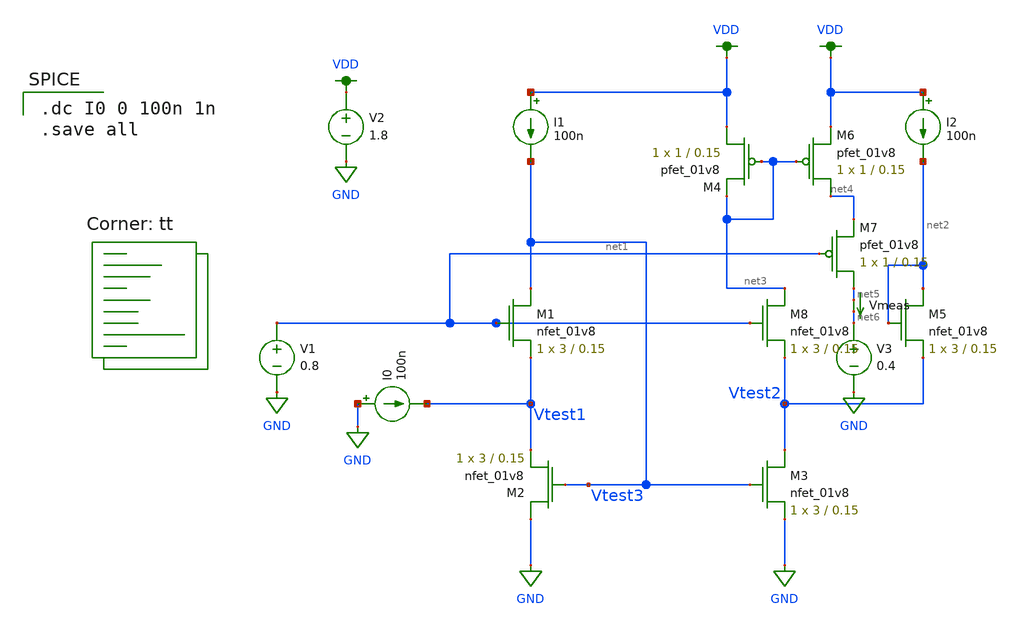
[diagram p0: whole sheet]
** sch_path: test_fvfccm.sch
**.subckt test_fvfccm
XM1 Vtest3 net1 Vtest1 GND sky130_fd_pr__nfet_01v8 L=0.15 W=3 nf=1 ad='int((nf+1)/2) * W/nf * 0.29' as='int((nf+2)/2) * W/nf * 0.29'
+ pd='2*int((nf+1)/2) * (W/nf + 0.29)' ps='2*int((nf+2)/2) * (W/nf + 0.29)' nrd='0.29 / W' nrs='0.29 / W'
+ sa=0 sb=0 sd=0 mult=1 m=1
XM2 GND Vtest3 Vtest1 GND sky130_fd_pr__nfet_01v8 L=0.15 W=3 nf=1 ad='int((nf+1)/2) * W/nf * 0.29' as='int((nf+2)/2) * W/nf * 0.29'
+ pd='2*int((nf+1)/2) * (W/nf + 0.29)' ps='2*int((nf+2)/2) * (W/nf + 0.29)' nrd='0.29 / W' nrs='0.29 / W'
+ sa=0 sb=0 sd=0 mult=1 m=1
I0 GND Vtest1 100n
V1 net1 GND 0.8
I1 VDD Vtest3 100n
V2 VDD GND 1.8
XM3 Vtest2 Vtest3 GND GND sky130_fd_pr__nfet_01v8 L=0.15 W=3 nf=1 ad='int((nf+1)/2) * W/nf * 0.29' as='int((nf+2)/2) * W/nf * 0.29'
+ pd='2*int((nf+1)/2) * (W/nf + 0.29)' ps='2*int((nf+2)/2) * (W/nf + 0.29)' nrd='0.29 / W' nrs='0.29 / W'
+ sa=0 sb=0 sd=0 mult=1 m=1
XM5 net2 net2 Vtest2 GND sky130_fd_pr__nfet_01v8 L=0.15 W=3 nf=1 ad='int((nf+1)/2) * W/nf * 0.29' as='int((nf+2)/2) * W/nf * 0.29'
+ pd='2*int((nf+1)/2) * (W/nf + 0.29)' ps='2*int((nf+2)/2) * (W/nf + 0.29)' nrd='0.29 / W' nrs='0.29 / W'
+ sa=0 sb=0 sd=0 mult=1 m=1
I2 VDD net2 100n
Vmeas net5 net6 0
.save i(vmeas)
XM4 VDD net3 net3 VDD sky130_fd_pr__pfet_01v8 L=0.15 W=1 nf=1 ad='int((nf+1)/2) * W/nf * 0.29' as='int((nf+2)/2) * W/nf * 0.29'
+ pd='2*int((nf+1)/2) * (W/nf + 0.29)' ps='2*int((nf+2)/2) * (W/nf + 0.29)' nrd='0.29 / W' nrs='0.29 / W'
+ sa=0 sb=0 sd=0 mult=1 m=1
XM6 net4 net3 VDD VDD sky130_fd_pr__pfet_01v8 L=0.15 W=1 nf=1 ad='int((nf+1)/2) * W/nf * 0.29' as='int((nf+2)/2) * W/nf * 0.29'
+ pd='2*int((nf+1)/2) * (W/nf + 0.29)' ps='2*int((nf+2)/2) * (W/nf + 0.29)' nrd='0.29 / W' nrs='0.29 / W'
+ sa=0 sb=0 sd=0 mult=1 m=1
XM7 net5 net1 net4 VDD sky130_fd_pr__pfet_01v8 L=0.15 W=1 nf=1 ad='int((nf+1)/2) * W/nf * 0.29' as='int((nf+2)/2) * W/nf * 0.29'
+ pd='2*int((nf+1)/2) * (W/nf + 0.29)' ps='2*int((nf+2)/2) * (W/nf + 0.29)' nrd='0.29 / W' nrs='0.29 / W'
+ sa=0 sb=0 sd=0 mult=1 m=1
V3 net6 GND 0.4
XM8 net3 net1 Vtest2 GND sky130_fd_pr__nfet_01v8 L=0.15 W=3 nf=1 ad='int((nf+1)/2) * W/nf * 0.29' as='int((nf+2)/2) * W/nf * 0.29'
+ pd='2*int((nf+1)/2) * (W/nf + 0.29)' ps='2*int((nf+2)/2) * (W/nf + 0.29)' nrd='0.29 / W' nrs='0.29 / W'
+ sa=0 sb=0 sd=0 mult=1 m=1
**** begin user architecture code

.dc I0 0 100n 1n
.save all

.lib $::SKYWATER_MODELS/sky130.lib.spice tt
**** end user architecture code
**.ends
.GLOBAL GND
.GLOBAL VDD
.end
